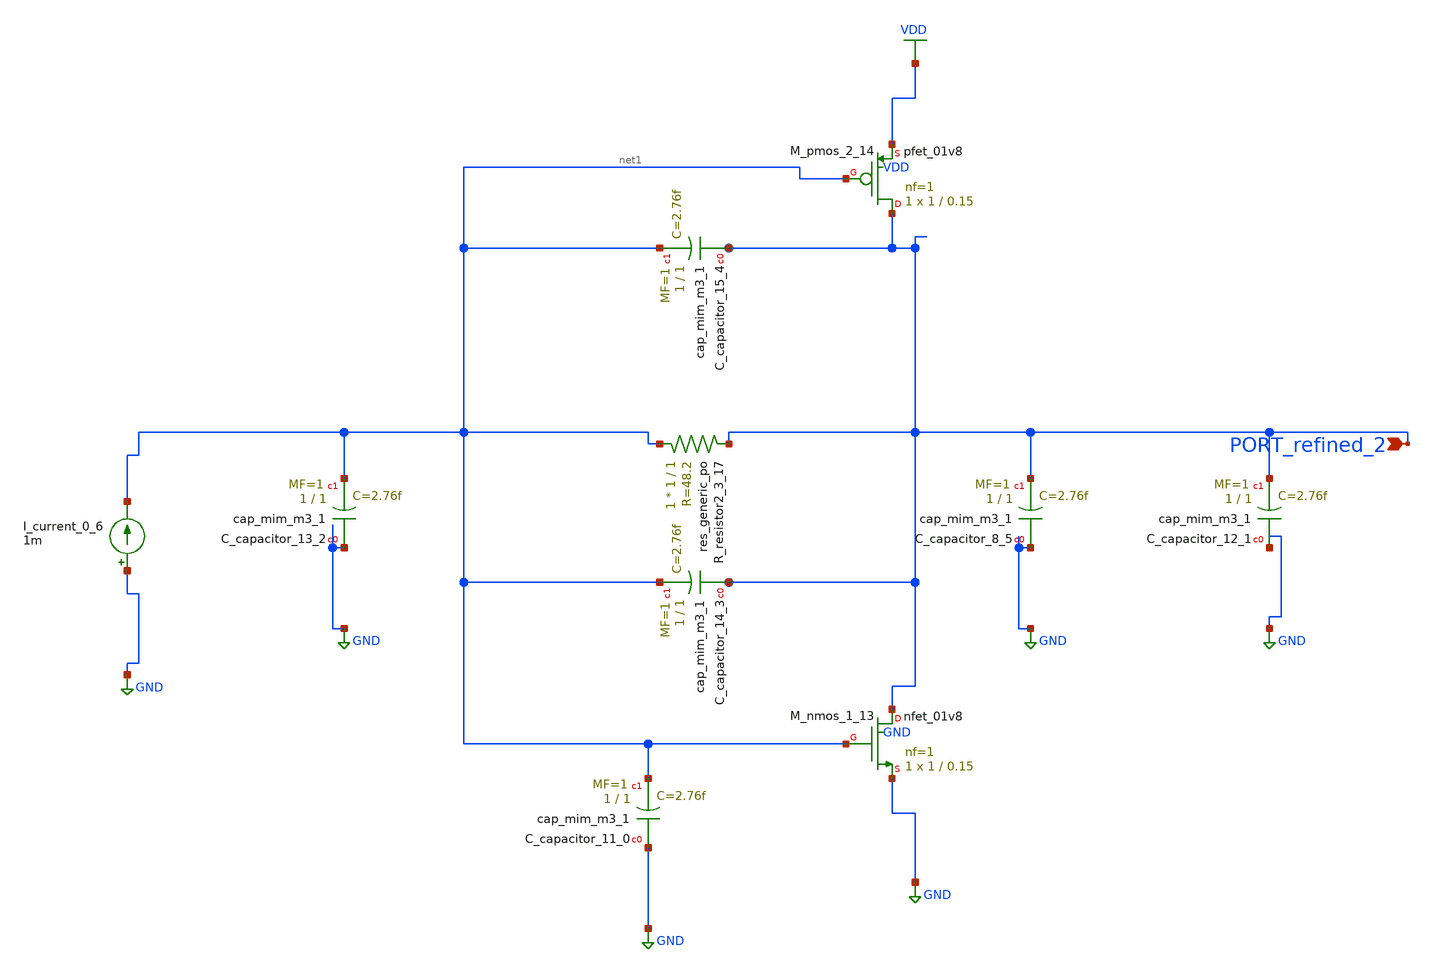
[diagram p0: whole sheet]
** sch_path: schematics/SchemGen/10_1109_OJCAS_2022_3164396_02_001_crop1.sch
**.subckt 10_1109_OJCAS_2022_3164396_02_001_crop1 PORT_refined_2
*.ipin PORT_refined_2
XC_capacitor_11_0 GND net1 sky130_fd_pr__cap_mim_m3_1 W=1 L=1 MF=1 m=1
XC_capacitor_12_1 GND PORT_refined_2 sky130_fd_pr__cap_mim_m3_1 W=1 L=1 MF=1 m=1
XC_capacitor_13_2 GND net1 sky130_fd_pr__cap_mim_m3_1 W=1 L=1 MF=1 m=1
XC_capacitor_14_3 PORT_refined_2 net1 sky130_fd_pr__cap_mim_m3_1 W=1 L=1 MF=1 m=1
XC_capacitor_15_4 PORT_refined_2 net1 sky130_fd_pr__cap_mim_m3_1 W=1 L=1 MF=1 m=1
XC_capacitor_8_5 GND PORT_refined_2 sky130_fd_pr__cap_mim_m3_1 W=1 L=1 MF=1 m=1
I_current_0_6 GND net1 1m
XM_nmos_1_13 PORT_refined_2 net1 GND GND sky130_fd_pr__nfet_01v8 L=0.15 W=1 nf=1 ad='int((1 + 1)/2) * 1 / 1 * 0.29'
+ as='int((1 + 2)/2) * 1 / 1 * 0.29' pd='2*int((1 + 1)/2) * (1 / 1 + 0.29)' ps='2*int((1 + 2)/2) * (1 / 1 + 0.29)'
+ nrd='0.29 / 1 ' nrs='0.29 / 1 ' sa=0 sb=0 sd=0 mult=1 m=1
XM_pmos_2_14 PORT_refined_2 net1 VDD VDD sky130_fd_pr__pfet_01v8 L=0.15 W=1 nf=1 ad='int((1 + 1)/2) * 1 / 1 * 0.29'
+ as='int((1 + 2)/2) * 1 / 1 * 0.29' pd='2*int((1 + 1)/2) * (1 / 1 + 0.29)' ps='2*int((1 + 2)/2) * (1 / 1 + 0.29)'
+ nrd='0.29 / 1 ' nrs='0.29 / 1 ' sa=0 sb=0 sd=0 mult=1 m=1
XR_resistor2_3_17 net1 PORT_refined_2 sky130_fd_pr__res_generic_po W=1 L=1 m=1
**.ends
.GLOBAL GND
.GLOBAL VDD
.end
